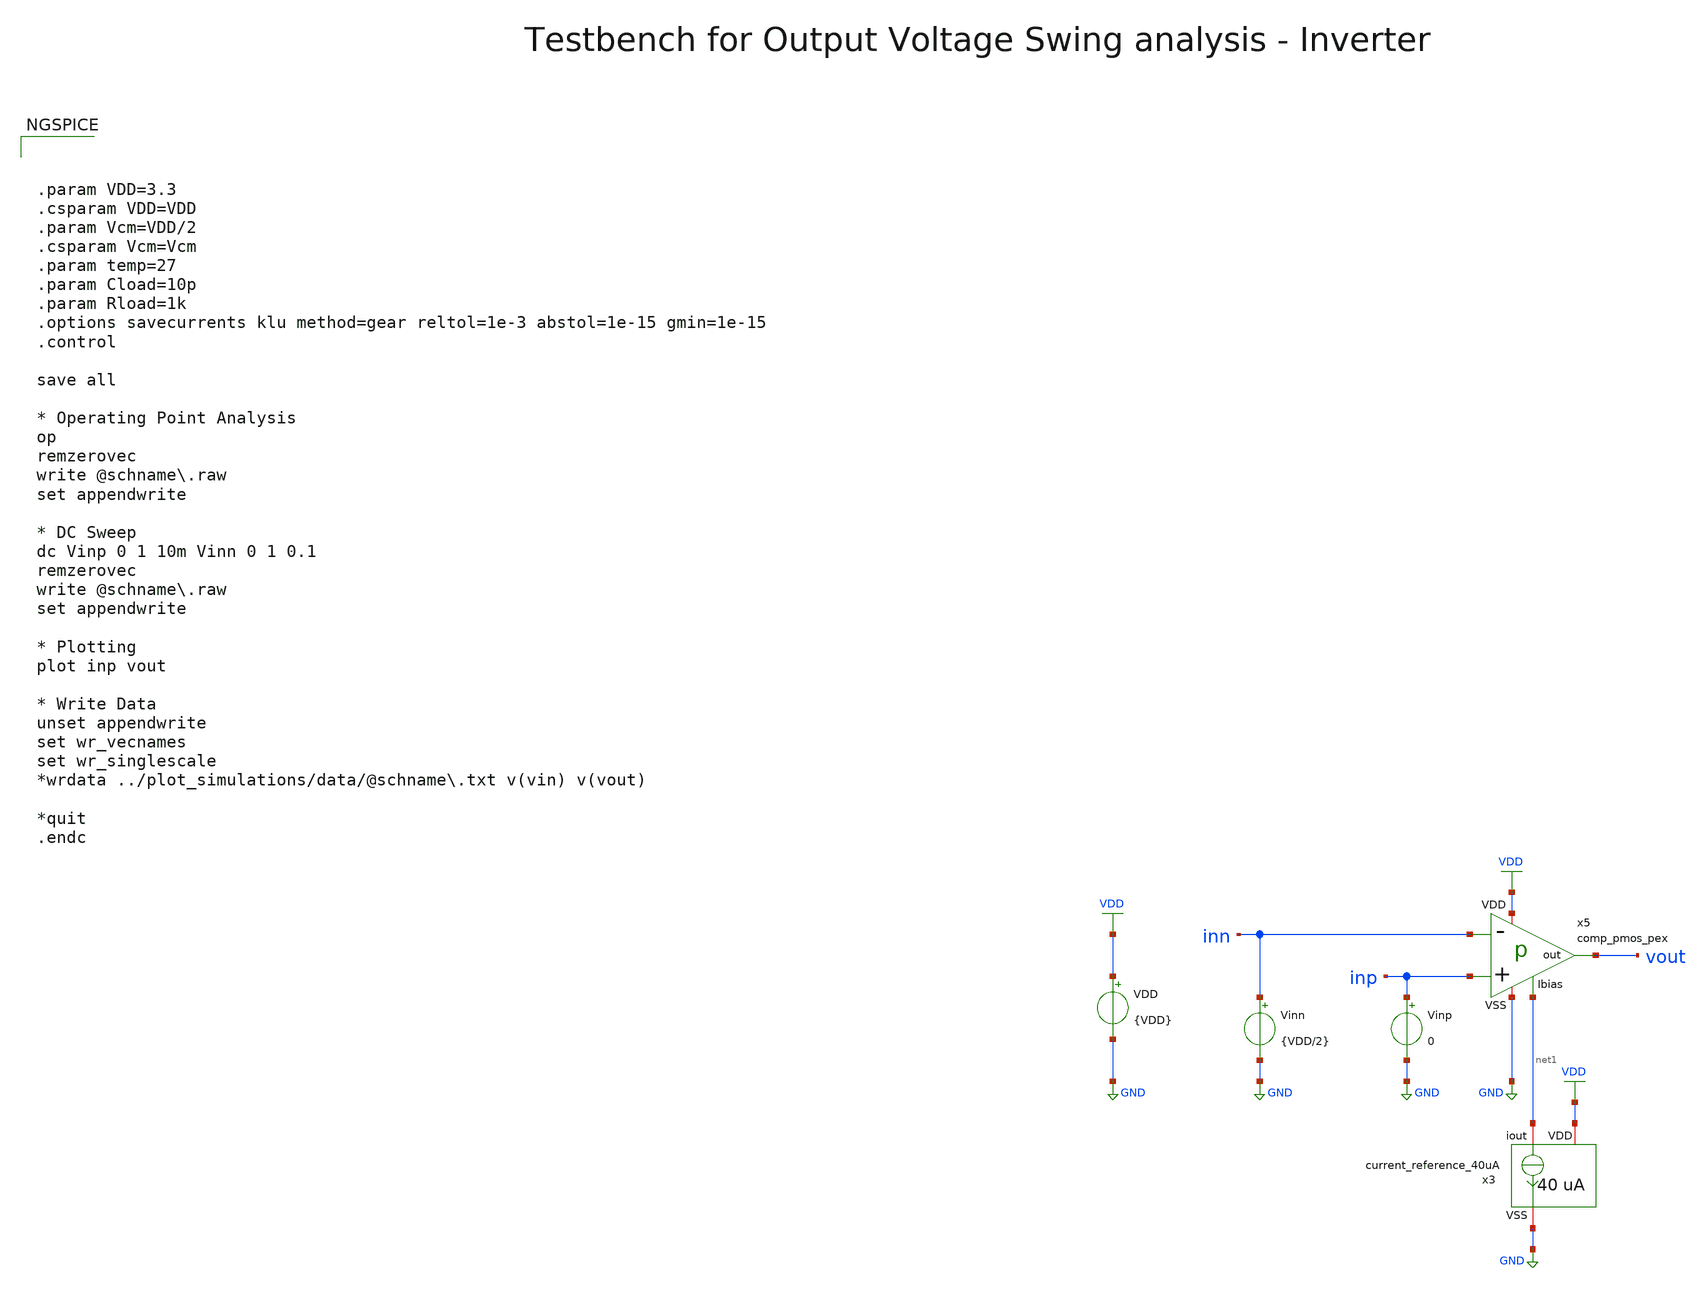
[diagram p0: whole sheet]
** sch_path: macros/heichips26_vcr/macros/switched_capacitor/testbenches/xschem/tb_comp_pmos_pex_dc.sch
**.subckt tb_comp_pmos_pex_dc
VDD VDD GND {VDD}
Vinp inp GND 0
Vinn inn GND {VDD/2}
x3 VDD net1 GND current_reference_40uA
x5 vout inn inp VDD net1 GND comp_pmos_pex
**** begin user architecture code



.param VDD=3.3
.csparam VDD=VDD
.param Vcm=VDD/2
.csparam Vcm=Vcm
.param temp=27
.param Cload=10p
.param Rload=1k
.options savecurrents klu method=gear reltol=1e-3 abstol=1e-15 gmin=1e-15
.control

save all

* Operating Point Analysis
op
remzerovec
write @schname\.raw
set appendwrite

* DC Sweep
dc Vinp 0 1 10m Vinn 0 1 0.1
remzerovec
write @schname\.raw
set appendwrite

* Plotting
plot inp vout

* Write Data
unset appendwrite
set wr_vecnames
set wr_singlescale
*wrdata ../plot_simulations/data/@schname\.txt v(vin) v(vout)

*quit
.endc



.lib cornerMOSlv.lib mos_tt
.lib cornerMOShv.lib mos_tt
.lib cornerRES.lib res_typ
.lib cornerDIO.lib dio_tt

**** end user architecture code
**.ends

* expanding   symbol:  current_reference_40uA.sym # of pins=3
** sym_path: macros/heichips26_vcr/macros/switched_capacitor/schematic/xschem/current_reference_40uA.sym
** sch_path: macros/heichips26_vcr/macros/switched_capacitor/schematic/xschem/current_reference_40uA.sch
.subckt current_reference_40uA VDD iout VSS
*.iopin VSS
*.iopin VDD
*.iopin iout
XM8 net2 net2 VSS VSS sg13_hv_nmos w=n_w l=n_l ng=1 m=1 mm_ok=1
XM6 net2 net1 VDD VDD sg13_hv_pmos w=p_w l=p_l ng=1 m=1 mm_ok=1
XM1 net1 net1 VDD VDD sg13_hv_pmos w=p_w l=p_l ng=1 m=1 mm_ok=1
XM3 net1 net2 net3 VSS sg13_hv_nmos w=n_w l=n_l ng=1 m=1 mm_ok=1
XR2 net4 VSS VSS rppd w=2e-6 l=21.9e-6 m=1 b=0 mm_ok=1
XM2 net1 net2 net3 VSS sg13_hv_nmos w=n_w l=n_l ng=1 m=1 mm_ok=1
XM4 net1 net2 net3 VSS sg13_hv_nmos w=n_w l=n_l ng=1 m=1 mm_ok=1
XM5 net1 net2 net3 VSS sg13_hv_nmos w=n_w l=n_l ng=1 m=1 mm_ok=1
XM7 iout net2 VSS VSS sg13_hv_nmos w=n_w l=n_l ng=1 m=1 mm_ok=1
XR3 net3 net4 VSS rsil w=0.5e-6 l=365e-6 m=1 mm_ok=1
**** begin user architecture code


.param n_w = 6u
.param n_l = 5u
.param p_w = 10u
.param p_l = 2u


**** end user architecture code
.ends

.GLOBAL GND
.GLOBAL VDD
.end
